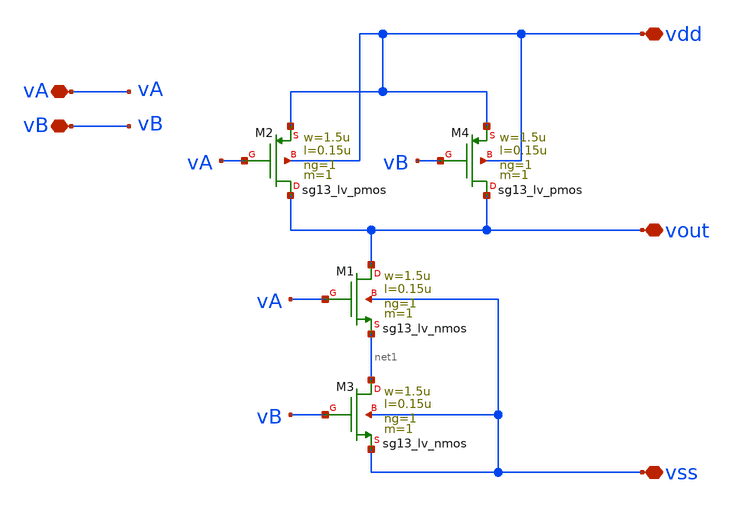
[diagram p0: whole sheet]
** sch_path: design/blocks/nandgate/schematic/nandgate.sch
**.subckt nandgate vout vA vB vdd vss
*.iopin vout
*.iopin vA
*.iopin vB
*.iopin vdd
*.iopin vss
XM1 vout vA net1 vss sg13_lv_nmos w=1.5u l=0.15u ng=1 m=1 mm_ok=1
XM2 vout vA vdd vdd sg13_lv_pmos w=1.5u l=0.15u ng=1 m=1 mm_ok=1
XM3 net1 vB vss vss sg13_lv_nmos w=1.5u l=0.15u ng=1 m=1 mm_ok=1
XM4 vout vB vdd vdd sg13_lv_pmos w=1.5u l=0.15u ng=1 m=1 mm_ok=1
**.ends
.end
